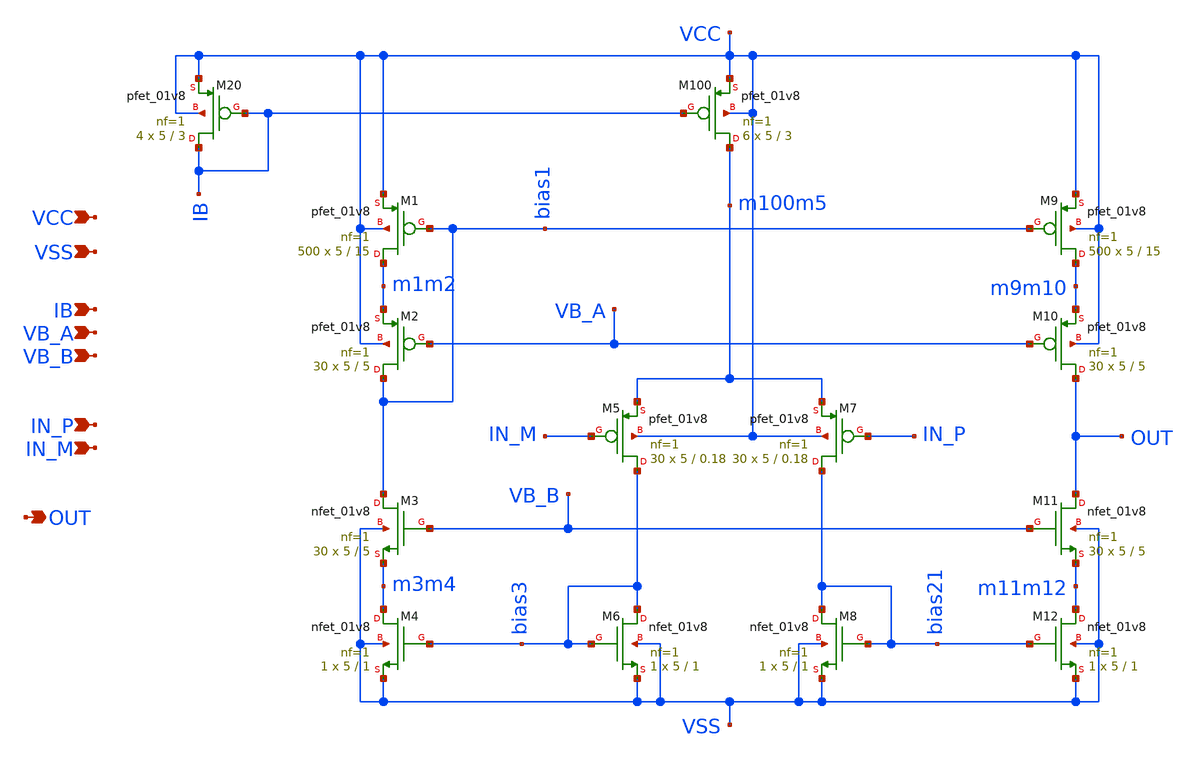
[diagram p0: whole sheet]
** sch_path: 01_IdeaDesign/opamp_cascode.sch
**.subckt opamp_cascode IN_P IN_M VCC VSS OUT VB_A VB_B IB
*.ipin IN_P
*.ipin IN_M
*.ipin VCC
*.ipin VSS
*.opin OUT
*.ipin VB_A
*.ipin VB_B
*.ipin IB
XM9 m9m10 bias1 VCC VCC sky130_fd_pr__pfet_01v8 L=15 W=5 nf=1 ad='int((nf+1)/2) * W/nf * 0.29' as='int((nf+2)/2) * W/nf * 0.29'
+ pd='2*int((nf+1)/2) * (W/nf + 0.29)' ps='2*int((nf+2)/2) * (W/nf + 0.29)' nrd='0.29 / W' nrs='0.29 / W'
+ sa=0 sb=0 sd=0 mult=500 m=500
XM1 m1m2 bias1 VCC VCC sky130_fd_pr__pfet_01v8 L=15 W=5 nf=1 ad='int((nf+1)/2) * W/nf * 0.29' as='int((nf+2)/2) * W/nf * 0.29'
+ pd='2*int((nf+1)/2) * (W/nf + 0.29)' ps='2*int((nf+2)/2) * (W/nf + 0.29)' nrd='0.29 / W' nrs='0.29 / W'
+ sa=0 sb=0 sd=0 mult=500 m=500
XM100 m100m5 IB VCC VCC sky130_fd_pr__pfet_01v8 L=3 W=5 nf=1 ad='int((nf+1)/2) * W/nf * 0.29' as='int((nf+2)/2) * W/nf * 0.29'
+ pd='2*int((nf+1)/2) * (W/nf + 0.29)' ps='2*int((nf+2)/2) * (W/nf + 0.29)' nrd='0.29 / W' nrs='0.29 / W'
+ sa=0 sb=0 sd=0 mult=6 m=6
XM20 IB IB VCC VCC sky130_fd_pr__pfet_01v8 L=3 W=5 nf=1 ad='int((nf+1)/2) * W/nf * 0.29' as='int((nf+2)/2) * W/nf * 0.29'
+ pd='2*int((nf+1)/2) * (W/nf + 0.29)' ps='2*int((nf+2)/2) * (W/nf + 0.29)' nrd='0.29 / W' nrs='0.29 / W'
+ sa=0 sb=0 sd=0 mult=4 m=4
XM10 OUT VB_A m9m10 VCC sky130_fd_pr__pfet_01v8 L=5 W=5 nf=1 ad='int((nf+1)/2) * W/nf * 0.29' as='int((nf+2)/2) * W/nf * 0.29'
+ pd='2*int((nf+1)/2) * (W/nf + 0.29)' ps='2*int((nf+2)/2) * (W/nf + 0.29)' nrd='0.29 / W' nrs='0.29 / W'
+ sa=0 sb=0 sd=0 mult=30 m=30
XM2 bias1 VB_A m1m2 VCC sky130_fd_pr__pfet_01v8 L=5 W=5 nf=1 ad='int((nf+1)/2) * W/nf * 0.29' as='int((nf+2)/2) * W/nf * 0.29'
+ pd='2*int((nf+1)/2) * (W/nf + 0.29)' ps='2*int((nf+2)/2) * (W/nf + 0.29)' nrd='0.29 / W' nrs='0.29 / W'
+ sa=0 sb=0 sd=0 mult=30 m=30
XM5 bias3 IN_M m100m5 VCC sky130_fd_pr__pfet_01v8 L=0.18 W=5 nf=1 ad='int((nf+1)/2) * W/nf * 0.29' as='int((nf+2)/2) * W/nf * 0.29'
+ pd='2*int((nf+1)/2) * (W/nf + 0.29)' ps='2*int((nf+2)/2) * (W/nf + 0.29)' nrd='0.29 / W' nrs='0.29 / W'
+ sa=0 sb=0 sd=0 mult=30 m=30
XM7 bias21 IN_P m100m5 VCC sky130_fd_pr__pfet_01v8 L=0.18 W=5 nf=1 ad='int((nf+1)/2) * W/nf * 0.29' as='int((nf+2)/2) * W/nf * 0.29'
+ pd='2*int((nf+1)/2) * (W/nf + 0.29)' ps='2*int((nf+2)/2) * (W/nf + 0.29)' nrd='0.29 / W' nrs='0.29 / W'
+ sa=0 sb=0 sd=0 mult=30 m=30
XM6 bias3 bias3 VSS VSS sky130_fd_pr__nfet_01v8 L=1 W=5 nf=1 ad='int((nf+1)/2) * W/nf * 0.29' as='int((nf+2)/2) * W/nf * 0.29'
+ pd='2*int((nf+1)/2) * (W/nf + 0.29)' ps='2*int((nf+2)/2) * (W/nf + 0.29)' nrd='0.29 / W' nrs='0.29 / W'
+ sa=0 sb=0 sd=0 mult=1 m=1
XM8 bias21 bias21 VSS VSS sky130_fd_pr__nfet_01v8 L=1 W=5 nf=1 ad='int((nf+1)/2) * W/nf * 0.29' as='int((nf+2)/2) * W/nf * 0.29'
+ pd='2*int((nf+1)/2) * (W/nf + 0.29)' ps='2*int((nf+2)/2) * (W/nf + 0.29)' nrd='0.29 / W' nrs='0.29 / W'
+ sa=0 sb=0 sd=0 mult=1 m=1
XM12 m11m12 bias21 VSS VSS sky130_fd_pr__nfet_01v8 L=1 W=5 nf=1 ad='int((nf+1)/2) * W/nf * 0.29' as='int((nf+2)/2) * W/nf * 0.29'
+ pd='2*int((nf+1)/2) * (W/nf + 0.29)' ps='2*int((nf+2)/2) * (W/nf + 0.29)' nrd='0.29 / W' nrs='0.29 / W'
+ sa=0 sb=0 sd=0 mult=1 m=1
XM4 m3m4 bias3 VSS VSS sky130_fd_pr__nfet_01v8 L=1 W=5 nf=1 ad='int((nf+1)/2) * W/nf * 0.29' as='int((nf+2)/2) * W/nf * 0.29'
+ pd='2*int((nf+1)/2) * (W/nf + 0.29)' ps='2*int((nf+2)/2) * (W/nf + 0.29)' nrd='0.29 / W' nrs='0.29 / W'
+ sa=0 sb=0 sd=0 mult=1 m=1
XM11 OUT VB_B m11m12 VSS sky130_fd_pr__nfet_01v8 L=5 W=5 nf=1 ad='int((nf+1)/2) * W/nf * 0.29' as='int((nf+2)/2) * W/nf * 0.29'
+ pd='2*int((nf+1)/2) * (W/nf + 0.29)' ps='2*int((nf+2)/2) * (W/nf + 0.29)' nrd='0.29 / W' nrs='0.29 / W'
+ sa=0 sb=0 sd=0 mult=30 m=30
XM3 bias1 VB_B m3m4 VSS sky130_fd_pr__nfet_01v8 L=5 W=5 nf=1 ad='int((nf+1)/2) * W/nf * 0.29' as='int((nf+2)/2) * W/nf * 0.29'
+ pd='2*int((nf+1)/2) * (W/nf + 0.29)' ps='2*int((nf+2)/2) * (W/nf + 0.29)' nrd='0.29 / W' nrs='0.29 / W'
+ sa=0 sb=0 sd=0 mult=30 m=30
**.ends
.end
